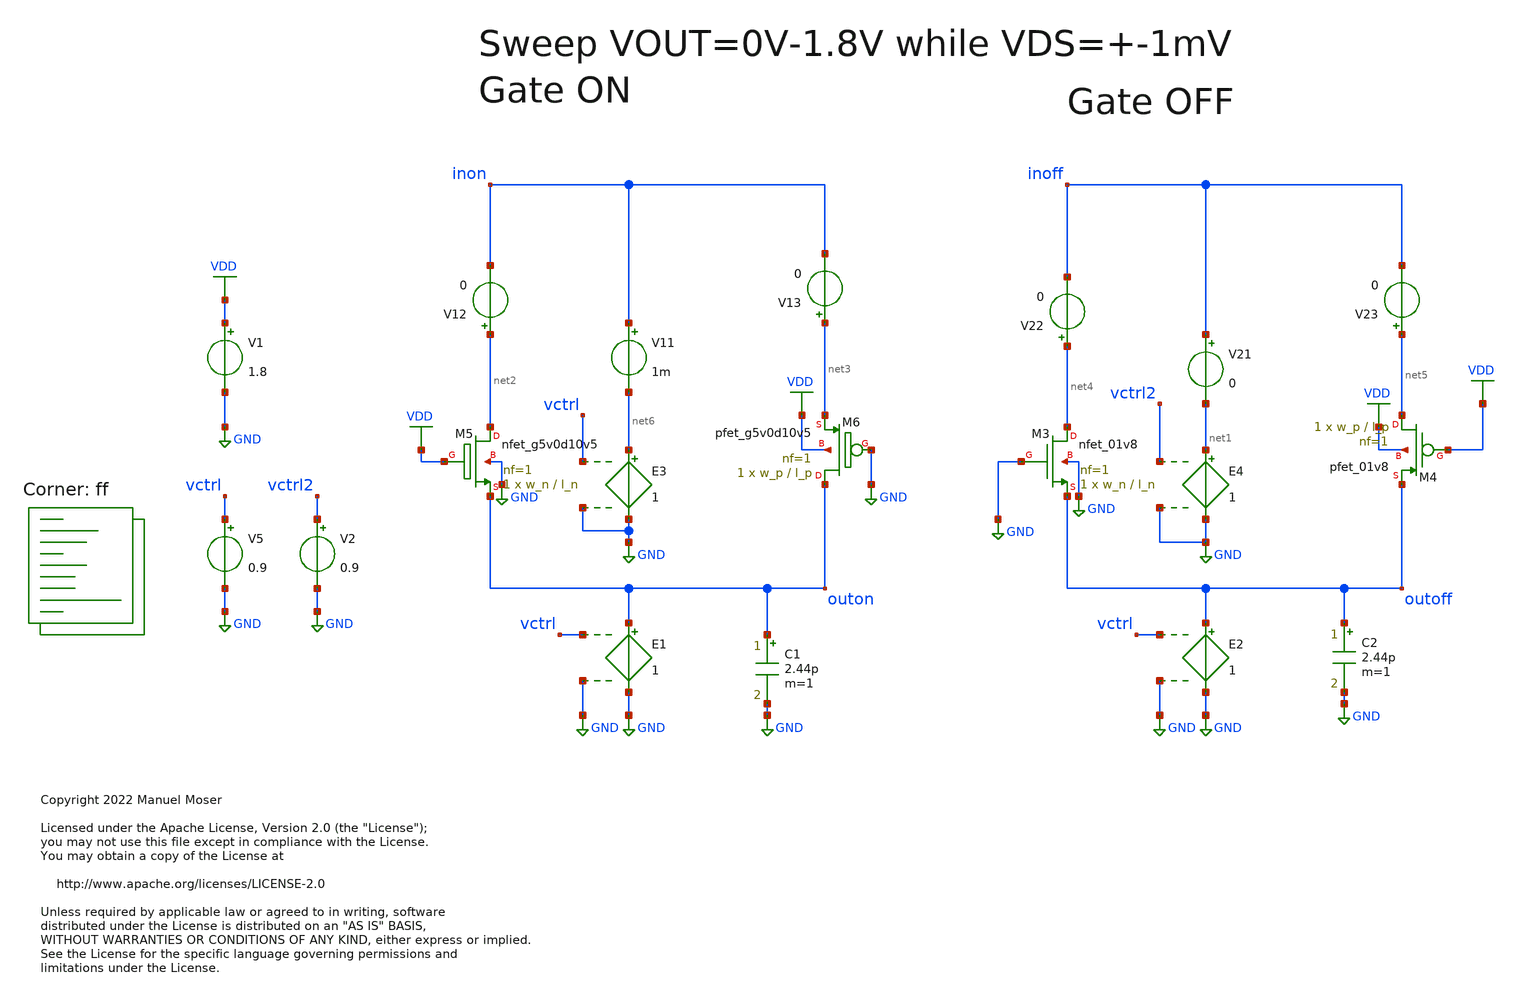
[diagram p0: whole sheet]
** sch_path: xschem/adc_gate_tb_resistance_g5v0.sch
* Copyright 2022 Manuel Moser
* Licensed under the Apache License, Version 2.0 (the "License");
**.subckt adc_gate_tb_resistance_g5v0
V5 vctrl GND 0.9
XM3 net4 GND outoff GND sky130_fd_pr__nfet_01v8 L=l_n W=w_n nf=1 ad='int((nf+1)/2) * W/nf * 0.29' as='int((nf+2)/2) * W/nf * 0.29'
+ pd='2*int((nf+1)/2) * (W/nf + 0.29)' ps='2*int((nf+2)/2) * (W/nf + 0.29)' nrd='0.29 / W' nrs='0.29 / W'
+ sa=0 sb=0 sd=0 mult=1 m=1
XM4 net5 VDD outoff VDD sky130_fd_pr__pfet_01v8 L=l_p W=w_p nf=1 ad='int((nf+1)/2) * W/nf * 0.29' as='int((nf+2)/2) * W/nf * 0.29'
+ pd='2*int((nf+1)/2) * (W/nf + 0.29)' ps='2*int((nf+2)/2) * (W/nf + 0.29)' nrd='0.29 / W' nrs='0.29 / W'
+ sa=0 sb=0 sd=0 mult=1 m=1
E1 outon GND vctrl GND 1
E2 outoff GND vctrl GND 1
C1 outon GND 2.44p m=1
C2 outoff GND 2.44p m=1
E3 net6 GND vctrl GND 1
E4 net1 GND vctrl2 GND 1
V21 inoff net1 0
V11 inon net6 1m
V12 net2 inon 0
V13 net3 inon 0
V22 net4 inoff 0
V23 net5 inoff 0
V1 VDD GND 1.8
XM5 net2 VDD outon GND sky130_fd_pr__nfet_g5v0d10v5 L=l_n W=w_n nf=1 ad='int((nf+1)/2) * W/nf * 0.29'
+ as='int((nf+2)/2) * W/nf * 0.29' pd='2*int((nf+1)/2) * (W/nf + 0.29)' ps='2*int((nf+2)/2) * (W/nf + 0.29)'
+ nrd='0.29 / W' nrs='0.29 / W' sa=0 sb=0 sd=0 mult=1 m=1
XM6 outon GND net3 VDD sky130_fd_pr__pfet_g5v0d10v5 L=l_p W=w_p nf=1 ad='int((nf+1)/2) * W/nf * 0.29'
+ as='int((nf+2)/2) * W/nf * 0.29' pd='2*int((nf+1)/2) * (W/nf + 0.29)' ps='2*int((nf+2)/2) * (W/nf + 0.29)'
+ nrd='0.29 / W' nrs='0.29 / W' sa=0 sb=0 sd=0 mult=1 m=1
V2 vctrl2 GND 0.9
**** begin user architecture code
.lib $::SKYWATER_MODELS/sky130.lib.spice ff


.save all
.temp = 100
*.options method=gear
.OPTIONS savecurrents
*.OPTIONS RELTOL=.1 TRTOL=1 ABSTOL=1e-20 CHGTOL=1.0e-20 DEFAD=1.0e-18
.save @m.x1.xm1.msky130_fd_pr__pfet_01v8[gm]
.save @m.x1.xm1.msky130_fd_pr__pfet_01v8[CGS]
.save @m.x1.xm1.msky130_fd_pr__pfet_01v8[Vth]
.save @m.x1.xm2.msky130_fd_pr__nfet_01v8_lvt[gm]
.save @m.x1.xm2.msky130_fd_pr__nfet_01v8_lvt[CGS]
.save @m.x1.xm2.msky130_fd_pr__nfet_01v8_lvt[Vth]

.param w_p=1
.param l_p = 0.5
.param w_n=1
.param l_n=0.5

.dc V5 100m 1.7 10m V2 0 1.8 900m

*********************************************************

.control
alterparam w_p=1
alterparam l_p=0.5
alterparam w_n=1
alterparam l_n=0.5

reset
run
write dc-sweep.out I(v11) I(v12) I(v13) I(v21) I(v22) I(v23) v(inon) v(outon) v(inoff) v(outoff)
set appendwrite

*********************************************************

alterparam w_p=4
alterparam l_p=0.5
alterparam w_n=4
alterparam l_n=0.5

reset
run
write dc-sweep.out I(v11) I(v12) I(v13) I(v21) I(v22) I(v23) v(inon) v(outon) v(inoff) v(outoff)
set appendwrite


*********************************************************

alterparam w_p=16
alterparam l_p=0.5
alterparam w_n=16
alterparam l_n=0.5

reset
run
write dc-sweep.out I(v11) I(v12) I(v13) I(v21) I(v22) I(v23) v(inon) v(outon) v(inoff) v(outoff)
set appendwrite

*********************************************************

*On-Resistance
plot (-(dc1.v(inon)-dc1.v(outon))/dc1.I(v11)) (-(dc2.v(inon)-dc2.v(outon))/dc2.I(v11)) (-(dc3.v(inon)-dc3.v(outon))/dc3.I(v11))
+ ylog xlabel 'Vout' ylabel 'R_in_Ohm' title 'RON Thickoxide-FET with VDS=1mV'

*Off-Resistance
plot (-dc1.I(v21)) (-dc2.I(v21)) (-dc3.I(v21)) xlabel 'output voltage' ylabel 'Current in Ampere' title
+ 'leakage current with VDS=1mV'

.endc


**** end user architecture code
**.ends
.GLOBAL GND
.GLOBAL VDD
.end
